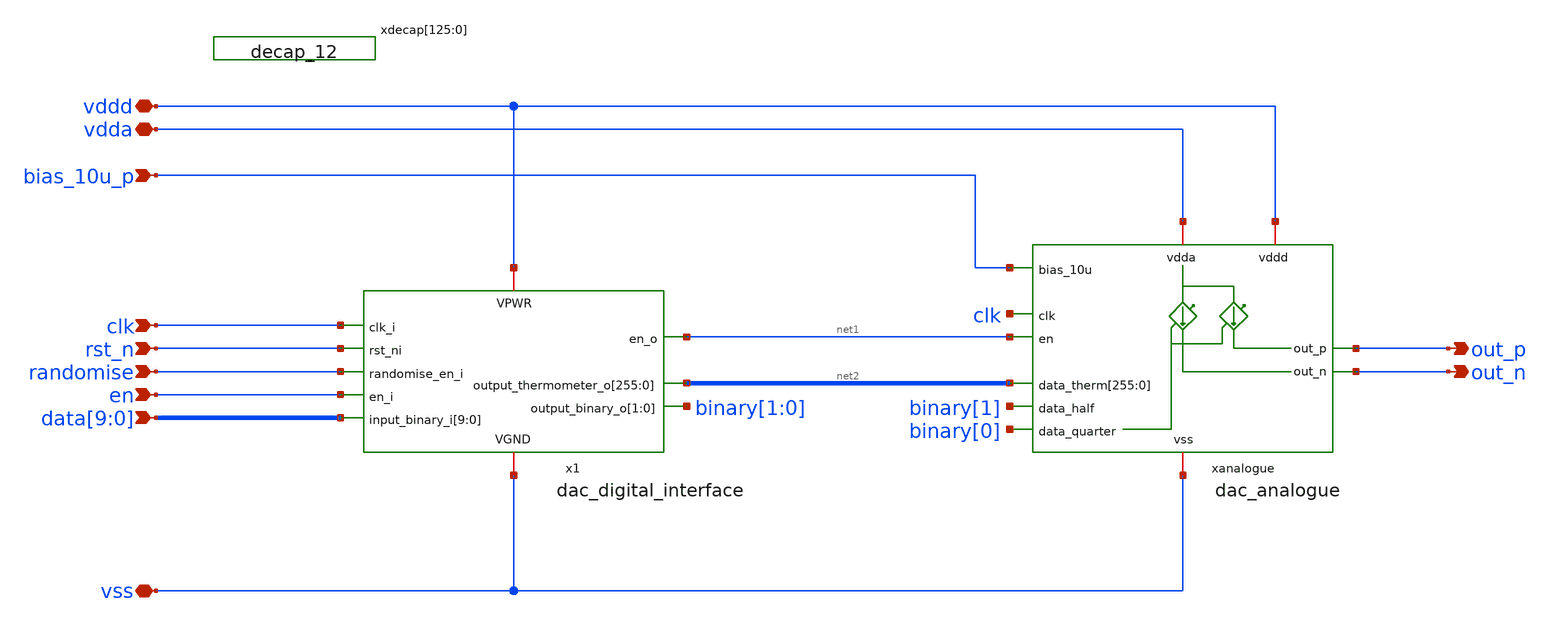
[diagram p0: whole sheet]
** sch_path: design/dac/dac.sch
**.subckt dac vss vdda vddd bias_10u_p clk
*+ data[9],data[8],data[7],data[6],data[5],data[4],data[3],data[2],data[1],data[0] out_p out_n en randomise rst_n
*.iopin vss
*.iopin vdda
*.iopin vddd
*.ipin bias_10u_p
*.ipin clk
*.ipin data[9],data[8],data[7],data[6],data[5],data[4],data[3],data[2],data[1],data[0]
*.opin out_p
*.opin out_n
*.ipin en
*.ipin randomise
*.ipin rst_n
xanalogue vdda vddd bias_10u_p clk net1 net2[255] net2[254] net2[253] net2[252] net2[251] net2[250]
+ net2[249] net2[248] net2[247] net2[246] net2[245] net2[244] net2[243] net2[242] net2[241] net2[240] net2[239]
+ net2[238] net2[237] net2[236] net2[235] net2[234] net2[233] net2[232] net2[231] net2[230] net2[229] net2[228]
+ net2[227] net2[226] net2[225] net2[224] net2[223] net2[222] net2[221] net2[220] net2[219] net2[218] net2[217]
+ net2[216] net2[215] net2[214] net2[213] net2[212] net2[211] net2[210] net2[209] net2[208] net2[207] net2[206]
+ net2[205] net2[204] net2[203] net2[202] net2[201] net2[200] net2[199] net2[198] net2[197] net2[196] net2[195]
+ net2[194] net2[193] net2[192] net2[191] net2[190] net2[189] net2[188] net2[187] net2[186] net2[185] net2[184]
+ net2[183] net2[182] net2[181] net2[180] net2[179] net2[178] net2[177] net2[176] net2[175] net2[174] net2[173]
+ net2[172] net2[171] net2[170] net2[169] net2[168] net2[167] net2[166] net2[165] net2[164] net2[163] net2[162]
+ net2[161] net2[160] net2[159] net2[158] net2[157] net2[156] net2[155] net2[154] net2[153] net2[152] net2[151]
+ net2[150] net2[149] net2[148] net2[147] net2[146] net2[145] net2[144] net2[143] net2[142] net2[141] net2[140]
+ net2[139] net2[138] net2[137] net2[136] net2[135] net2[134] net2[133] net2[132] net2[131] net2[130] net2[129]
+ net2[128] net2[127] net2[126] net2[125] net2[124] net2[123] net2[122] net2[121] net2[120] net2[119] net2[118]
+ net2[117] net2[116] net2[115] net2[114] net2[113] net2[112] net2[111] net2[110] net2[109] net2[108] net2[107]
+ net2[106] net2[105] net2[104] net2[103] net2[102] net2[101] net2[100] net2[99] net2[98] net2[97] net2[96]
+ net2[95] net2[94] net2[93] net2[92] net2[91] net2[90] net2[89] net2[88] net2[87] net2[86] net2[85] net2[84]
+ net2[83] net2[82] net2[81] net2[80] net2[79] net2[78] net2[77] net2[76] net2[75] net2[74] net2[73] net2[72]
+ net2[71] net2[70] net2[69] net2[68] net2[67] net2[66] net2[65] net2[64] net2[63] net2[62] net2[61] net2[60]
+ net2[59] net2[58] net2[57] net2[56] net2[55] net2[54] net2[53] net2[52] net2[51] net2[50] net2[49] net2[48]
+ net2[47] net2[46] net2[45] net2[44] net2[43] net2[42] net2[41] net2[40] net2[39] net2[38] net2[37] net2[36]
+ net2[35] net2[34] net2[33] net2[32] net2[31] net2[30] net2[29] net2[28] net2[27] net2[26] net2[25] net2[24]
+ net2[23] net2[22] net2[21] net2[20] net2[19] net2[18] net2[17] net2[16] net2[15] net2[14] net2[13] net2[12]
+ net2[11] net2[10] net2[9] net2[8] net2[7] net2[6] net2[5] net2[4] net2[3] net2[2] net2[1] net2[0] binary[1]
+ binary[0] out_p out_n vss dac_analogue
x1 vddd clk net2[255] net2[254] net2[253] net2[252] net2[251] net2[250] net2[249] net2[248]
+ net2[247] net2[246] net2[245] net2[244] net2[243] net2[242] net2[241] net2[240] net2[239] net2[238] net2[237]
+ net2[236] net2[235] net2[234] net2[233] net2[232] net2[231] net2[230] net2[229] net2[228] net2[227] net2[226]
+ net2[225] net2[224] net2[223] net2[222] net2[221] net2[220] net2[219] net2[218] net2[217] net2[216] net2[215]
+ net2[214] net2[213] net2[212] net2[211] net2[210] net2[209] net2[208] net2[207] net2[206] net2[205] net2[204]
+ net2[203] net2[202] net2[201] net2[200] net2[199] net2[198] net2[197] net2[196] net2[195] net2[194] net2[193]
+ net2[192] net2[191] net2[190] net2[189] net2[188] net2[187] net2[186] net2[185] net2[184] net2[183] net2[182]
+ net2[181] net2[180] net2[179] net2[178] net2[177] net2[176] net2[175] net2[174] net2[173] net2[172] net2[171]
+ net2[170] net2[169] net2[168] net2[167] net2[166] net2[165] net2[164] net2[163] net2[162] net2[161] net2[160]
+ net2[159] net2[158] net2[157] net2[156] net2[155] net2[154] net2[153] net2[152] net2[151] net2[150] net2[149]
+ net2[148] net2[147] net2[146] net2[145] net2[144] net2[143] net2[142] net2[141] net2[140] net2[139] net2[138]
+ net2[137] net2[136] net2[135] net2[134] net2[133] net2[132] net2[131] net2[130] net2[129] net2[128] net2[127]
+ net2[126] net2[125] net2[124] net2[123] net2[122] net2[121] net2[120] net2[119] net2[118] net2[117] net2[116]
+ net2[115] net2[114] net2[113] net2[112] net2[111] net2[110] net2[109] net2[108] net2[107] net2[106] net2[105]
+ net2[104] net2[103] net2[102] net2[101] net2[100] net2[99] net2[98] net2[97] net2[96] net2[95] net2[94]
+ net2[93] net2[92] net2[91] net2[90] net2[89] net2[88] net2[87] net2[86] net2[85] net2[84] net2[83] net2[82]
+ net2[81] net2[80] net2[79] net2[78] net2[77] net2[76] net2[75] net2[74] net2[73] net2[72] net2[71] net2[70]
+ net2[69] net2[68] net2[67] net2[66] net2[65] net2[64] net2[63] net2[62] net2[61] net2[60] net2[59] net2[58]
+ net2[57] net2[56] net2[55] net2[54] net2[53] net2[52] net2[51] net2[50] net2[49] net2[48] net2[47] net2[46]
+ net2[45] net2[44] net2[43] net2[42] net2[41] net2[40] net2[39] net2[38] net2[37] net2[36] net2[35] net2[34]
+ net2[33] net2[32] net2[31] net2[30] net2[29] net2[28] net2[27] net2[26] net2[25] net2[24] net2[23] net2[22]
+ net2[21] net2[20] net2[19] net2[18] net2[17] net2[16] net2[15] net2[14] net2[13] net2[12] net2[11] net2[10]
+ net2[9] net2[8] net2[7] net2[6] net2[5] net2[4] net2[3] net2[2] net2[1] net2[0] rst_n binary[1] binary[0]
+ randomise net1 en data[9] data[8] data[7] data[6] data[5] data[4] data[3] data[2] data[1] data[0] vss
+ dac_digital_interface
xdecap[125] vss vss vdda vdda sky130_fd_sc_hd__decap_12
xdecap[124] vss vss vdda vdda sky130_fd_sc_hd__decap_12
xdecap[123] vss vss vdda vdda sky130_fd_sc_hd__decap_12
xdecap[122] vss vss vdda vdda sky130_fd_sc_hd__decap_12
xdecap[121] vss vss vdda vdda sky130_fd_sc_hd__decap_12
xdecap[120] vss vss vdda vdda sky130_fd_sc_hd__decap_12
xdecap[119] vss vss vdda vdda sky130_fd_sc_hd__decap_12
xdecap[118] vss vss vdda vdda sky130_fd_sc_hd__decap_12
xdecap[117] vss vss vdda vdda sky130_fd_sc_hd__decap_12
xdecap[116] vss vss vdda vdda sky130_fd_sc_hd__decap_12
xdecap[115] vss vss vdda vdda sky130_fd_sc_hd__decap_12
xdecap[114] vss vss vdda vdda sky130_fd_sc_hd__decap_12
xdecap[113] vss vss vdda vdda sky130_fd_sc_hd__decap_12
xdecap[112] vss vss vdda vdda sky130_fd_sc_hd__decap_12
xdecap[111] vss vss vdda vdda sky130_fd_sc_hd__decap_12
xdecap[110] vss vss vdda vdda sky130_fd_sc_hd__decap_12
xdecap[109] vss vss vdda vdda sky130_fd_sc_hd__decap_12
xdecap[108] vss vss vdda vdda sky130_fd_sc_hd__decap_12
xdecap[107] vss vss vdda vdda sky130_fd_sc_hd__decap_12
xdecap[106] vss vss vdda vdda sky130_fd_sc_hd__decap_12
xdecap[105] vss vss vdda vdda sky130_fd_sc_hd__decap_12
xdecap[104] vss vss vdda vdda sky130_fd_sc_hd__decap_12
xdecap[103] vss vss vdda vdda sky130_fd_sc_hd__decap_12
xdecap[102] vss vss vdda vdda sky130_fd_sc_hd__decap_12
xdecap[101] vss vss vdda vdda sky130_fd_sc_hd__decap_12
xdecap[100] vss vss vdda vdda sky130_fd_sc_hd__decap_12
xdecap[99] vss vss vdda vdda sky130_fd_sc_hd__decap_12
xdecap[98] vss vss vdda vdda sky130_fd_sc_hd__decap_12
xdecap[97] vss vss vdda vdda sky130_fd_sc_hd__decap_12
xdecap[96] vss vss vdda vdda sky130_fd_sc_hd__decap_12
xdecap[95] vss vss vdda vdda sky130_fd_sc_hd__decap_12
xdecap[94] vss vss vdda vdda sky130_fd_sc_hd__decap_12
xdecap[93] vss vss vdda vdda sky130_fd_sc_hd__decap_12
xdecap[92] vss vss vdda vdda sky130_fd_sc_hd__decap_12
xdecap[91] vss vss vdda vdda sky130_fd_sc_hd__decap_12
xdecap[90] vss vss vdda vdda sky130_fd_sc_hd__decap_12
xdecap[89] vss vss vdda vdda sky130_fd_sc_hd__decap_12
xdecap[88] vss vss vdda vdda sky130_fd_sc_hd__decap_12
xdecap[87] vss vss vdda vdda sky130_fd_sc_hd__decap_12
xdecap[86] vss vss vdda vdda sky130_fd_sc_hd__decap_12
xdecap[85] vss vss vdda vdda sky130_fd_sc_hd__decap_12
xdecap[84] vss vss vdda vdda sky130_fd_sc_hd__decap_12
xdecap[83] vss vss vdda vdda sky130_fd_sc_hd__decap_12
xdecap[82] vss vss vdda vdda sky130_fd_sc_hd__decap_12
xdecap[81] vss vss vdda vdda sky130_fd_sc_hd__decap_12
xdecap[80] vss vss vdda vdda sky130_fd_sc_hd__decap_12
xdecap[79] vss vss vdda vdda sky130_fd_sc_hd__decap_12
xdecap[78] vss vss vdda vdda sky130_fd_sc_hd__decap_12
xdecap[77] vss vss vdda vdda sky130_fd_sc_hd__decap_12
xdecap[76] vss vss vdda vdda sky130_fd_sc_hd__decap_12
xdecap[75] vss vss vdda vdda sky130_fd_sc_hd__decap_12
xdecap[74] vss vss vdda vdda sky130_fd_sc_hd__decap_12
xdecap[73] vss vss vdda vdda sky130_fd_sc_hd__decap_12
xdecap[72] vss vss vdda vdda sky130_fd_sc_hd__decap_12
xdecap[71] vss vss vdda vdda sky130_fd_sc_hd__decap_12
xdecap[70] vss vss vdda vdda sky130_fd_sc_hd__decap_12
xdecap[69] vss vss vdda vdda sky130_fd_sc_hd__decap_12
xdecap[68] vss vss vdda vdda sky130_fd_sc_hd__decap_12
xdecap[67] vss vss vdda vdda sky130_fd_sc_hd__decap_12
xdecap[66] vss vss vdda vdda sky130_fd_sc_hd__decap_12
xdecap[65] vss vss vdda vdda sky130_fd_sc_hd__decap_12
xdecap[64] vss vss vdda vdda sky130_fd_sc_hd__decap_12
xdecap[63] vss vss vdda vdda sky130_fd_sc_hd__decap_12
xdecap[62] vss vss vdda vdda sky130_fd_sc_hd__decap_12
xdecap[61] vss vss vdda vdda sky130_fd_sc_hd__decap_12
xdecap[60] vss vss vdda vdda sky130_fd_sc_hd__decap_12
xdecap[59] vss vss vdda vdda sky130_fd_sc_hd__decap_12
xdecap[58] vss vss vdda vdda sky130_fd_sc_hd__decap_12
xdecap[57] vss vss vdda vdda sky130_fd_sc_hd__decap_12
xdecap[56] vss vss vdda vdda sky130_fd_sc_hd__decap_12
xdecap[55] vss vss vdda vdda sky130_fd_sc_hd__decap_12
xdecap[54] vss vss vdda vdda sky130_fd_sc_hd__decap_12
xdecap[53] vss vss vdda vdda sky130_fd_sc_hd__decap_12
xdecap[52] vss vss vdda vdda sky130_fd_sc_hd__decap_12
xdecap[51] vss vss vdda vdda sky130_fd_sc_hd__decap_12
xdecap[50] vss vss vdda vdda sky130_fd_sc_hd__decap_12
xdecap[49] vss vss vdda vdda sky130_fd_sc_hd__decap_12
xdecap[48] vss vss vdda vdda sky130_fd_sc_hd__decap_12
xdecap[47] vss vss vdda vdda sky130_fd_sc_hd__decap_12
xdecap[46] vss vss vdda vdda sky130_fd_sc_hd__decap_12
xdecap[45] vss vss vdda vdda sky130_fd_sc_hd__decap_12
xdecap[44] vss vss vdda vdda sky130_fd_sc_hd__decap_12
xdecap[43] vss vss vdda vdda sky130_fd_sc_hd__decap_12
xdecap[42] vss vss vdda vdda sky130_fd_sc_hd__decap_12
xdecap[41] vss vss vdda vdda sky130_fd_sc_hd__decap_12
xdecap[40] vss vss vdda vdda sky130_fd_sc_hd__decap_12
xdecap[39] vss vss vdda vdda sky130_fd_sc_hd__decap_12
xdecap[38] vss vss vdda vdda sky130_fd_sc_hd__decap_12
xdecap[37] vss vss vdda vdda sky130_fd_sc_hd__decap_12
xdecap[36] vss vss vdda vdda sky130_fd_sc_hd__decap_12
xdecap[35] vss vss vdda vdda sky130_fd_sc_hd__decap_12
xdecap[34] vss vss vdda vdda sky130_fd_sc_hd__decap_12
xdecap[33] vss vss vdda vdda sky130_fd_sc_hd__decap_12
xdecap[32] vss vss vdda vdda sky130_fd_sc_hd__decap_12
xdecap[31] vss vss vdda vdda sky130_fd_sc_hd__decap_12
xdecap[30] vss vss vdda vdda sky130_fd_sc_hd__decap_12
xdecap[29] vss vss vdda vdda sky130_fd_sc_hd__decap_12
xdecap[28] vss vss vdda vdda sky130_fd_sc_hd__decap_12
xdecap[27] vss vss vdda vdda sky130_fd_sc_hd__decap_12
xdecap[26] vss vss vdda vdda sky130_fd_sc_hd__decap_12
xdecap[25] vss vss vdda vdda sky130_fd_sc_hd__decap_12
xdecap[24] vss vss vdda vdda sky130_fd_sc_hd__decap_12
xdecap[23] vss vss vdda vdda sky130_fd_sc_hd__decap_12
xdecap[22] vss vss vdda vdda sky130_fd_sc_hd__decap_12
xdecap[21] vss vss vdda vdda sky130_fd_sc_hd__decap_12
xdecap[20] vss vss vdda vdda sky130_fd_sc_hd__decap_12
xdecap[19] vss vss vdda vdda sky130_fd_sc_hd__decap_12
xdecap[18] vss vss vdda vdda sky130_fd_sc_hd__decap_12
xdecap[17] vss vss vdda vdda sky130_fd_sc_hd__decap_12
xdecap[16] vss vss vdda vdda sky130_fd_sc_hd__decap_12
xdecap[15] vss vss vdda vdda sky130_fd_sc_hd__decap_12
xdecap[14] vss vss vdda vdda sky130_fd_sc_hd__decap_12
xdecap[13] vss vss vdda vdda sky130_fd_sc_hd__decap_12
xdecap[12] vss vss vdda vdda sky130_fd_sc_hd__decap_12
xdecap[11] vss vss vdda vdda sky130_fd_sc_hd__decap_12
xdecap[10] vss vss vdda vdda sky130_fd_sc_hd__decap_12
xdecap[9] vss vss vdda vdda sky130_fd_sc_hd__decap_12
xdecap[8] vss vss vdda vdda sky130_fd_sc_hd__decap_12
xdecap[7] vss vss vdda vdda sky130_fd_sc_hd__decap_12
xdecap[6] vss vss vdda vdda sky130_fd_sc_hd__decap_12
xdecap[5] vss vss vdda vdda sky130_fd_sc_hd__decap_12
xdecap[4] vss vss vdda vdda sky130_fd_sc_hd__decap_12
xdecap[3] vss vss vdda vdda sky130_fd_sc_hd__decap_12
xdecap[2] vss vss vdda vdda sky130_fd_sc_hd__decap_12
xdecap[1] vss vss vdda vdda sky130_fd_sc_hd__decap_12
xdecap[0] vss vss vdda vdda sky130_fd_sc_hd__decap_12
**.ends
.end
